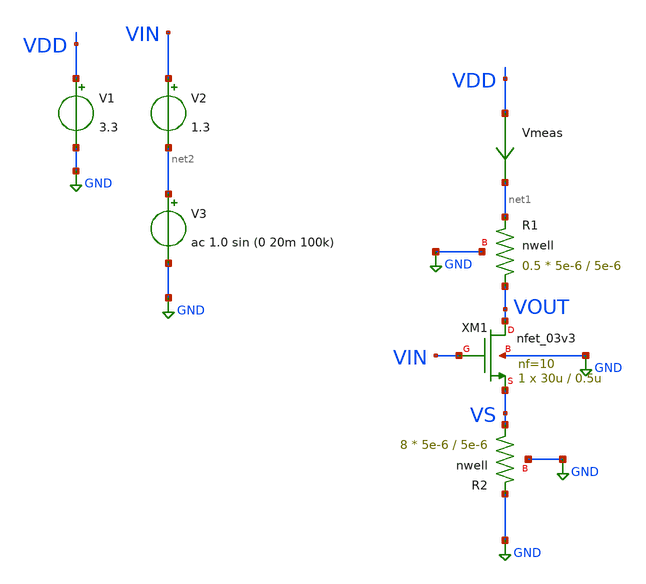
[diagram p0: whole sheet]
** sch_path: simple_amp4.sch
**.subckt simple_amp4
XM1 VOUT VIN VS GND nfet_03v3 L=0.5u W=30u nf=10 ad='int((nf+1)/2) * W/nf * 0.18u' as='int((nf+2)/2) * W/nf * 0.18u'
+ pd='2*int((nf+1)/2) * (W/nf + 0.18u)' ps='2*int((nf+2)/2) * (W/nf + 0.18u)' nrd='0.18u / W' nrs='0.18u / W'
+ sa=0 sb=0 sd=0 m=1
Vmeas VDD net1 0
.save i(vmeas)
V1 VDD GND 3.3
V2 VIN net2 1.3
XR1 VOUT net1 GND nwell r_width=5e-6 r_length=5e-6 m=0.5
XR2 VS GND GND nwell r_width=5e-6 r_length=5e-6 m=8
V3 net2 GND ac 1.0 sin (0 20m 100k)
**** begin user architecture code

.include $::180MCU_MODELS/design.ngspice
*.lib $::180MCU_MODELS/sm141064.ngspice statistical
*.lib $::180MCU_MODELS/sm141064.ngspice res_statistical
.lib $::180MCU_MODELS/sm141064.ngspice typical
.lib $::180MCU_MODELS/sm141064.ngspice res_typical
.lib $::180MCU_MODELS/sm141064.ngspice moscap_typical
.lib $::180MCU_MODELS/sm141064.ngspice bjt_typical
.lib $::180MCU_MODELS/sm141064.ngspice diode_typical
.lib $::180MCU_MODELS/sm141064.ngspice mimcap_typical
.TEMP 27

.param   sw_stat_global = 1   sw_stat_mism = 1  mc_skew = 3  res_mc_skew = 3  cap_mc_skew = 3
+  fnoicor = 1



.control
save all
dc V2 0 3.3 0.01


plot v(VOUT) deriv(v(VOUT)) v(VIN) (v(VIN)-v(VS)) (v(VOUT)-v(VS))
plot v(VOUT) deriv(v(VOUT))
plot i(Vmeas)
plot deriv(v(VOUT))
tran 10ns 20u
plot (v(VOUT)-1.37287) (v(VIN)-1.3)
plot fft((v(VOUT))) fft((v(VIN)))
ac dec 20 1 50G
plot v(VOUT)
.endc

**** end user architecture code
**.ends
.GLOBAL GND
.end
